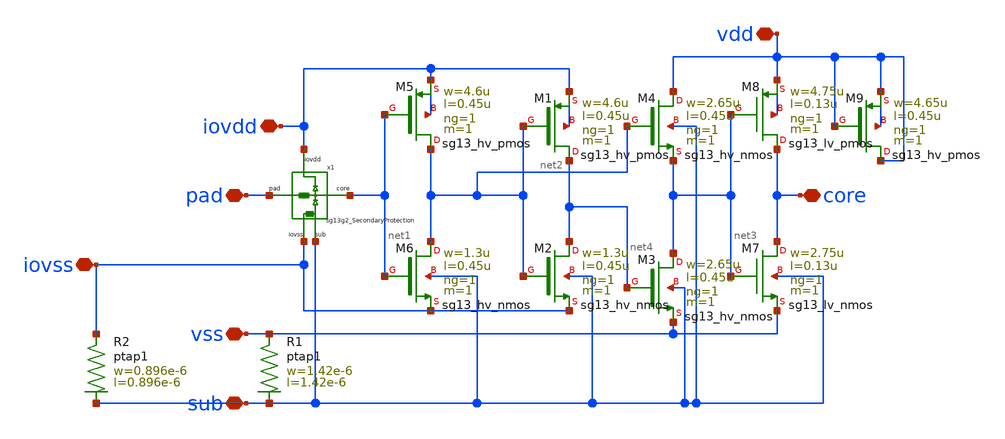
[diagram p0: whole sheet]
** sch_path: MSPHY6034-main/dependencies/unic_cass_2025_team04_padring/xschem/openpdk-libraries/ihp-sg13g2/sg13g2_io/xschem/sg13g2_LevelDown.sch
**.subckt sg13g2_LevelDown iovdd vss core pad vdd iovss sub
*.iopin iovdd
*.iopin vss
*.iopin core
*.iopin pad
*.iopin vdd
*.iopin iovss
*.iopin sub
XR1 vss sub ptap1 R=127.3 w=1.42e-6 l=1.42e-6
XM5 net2 net1 iovdd iovdd sg13_hv_pmos w=4.6u l=0.45u ng=1 m=1 mm_ok=1
XM6 net2 net1 iovss sub sg13_hv_nmos w=1.3u l=0.45u ng=1 m=1 mm_ok=1
XM7 core net3 vss sub sg13_lv_nmos w=2.75u l=0.13u ng=1 m=1 mm_ok=1
XM8 core net3 vdd vdd sg13_lv_pmos w=4.75u l=0.13u ng=1 m=1 mm_ok=1
x1 net1 iovdd iovss pad sub sg13g2_SecondaryProtection
XR2 iovss sub ptap1 R=223.4 w=0.896e-6 l=0.896e-6
XM1 net4 net2 iovdd iovdd sg13_hv_pmos w=4.6u l=0.45u ng=1 m=1 mm_ok=1
XM2 net4 net2 iovss sub sg13_hv_nmos w=1.3u l=0.45u ng=1 m=1 mm_ok=1
XM3 net3 net4 vss sub sg13_hv_nmos w=2.65u l=0.45u ng=1 m=1 mm_ok=1
XM4 vdd net2 net3 sub sg13_hv_nmos w=2.65u l=0.45u ng=1 m=1 mm_ok=1
XM9 vdd vdd vdd vdd sg13_hv_pmos w=4.65u l=0.45u ng=1 m=1 mm_ok=1
**.ends

* expanding   symbol:  sg13g2_SecondaryProtection.sym # of pins=5
** sym_path: MSPHY6034-main/schematic/xschem/openpdk-libraries/ihp-sg13g2/sg13g2_io/xschem/sg13g2_SecondaryProtection.sym
** sch_path: MSPHY6034-main/schematic/xschem/openpdk-libraries/ihp-sg13g2/sg13g2_io/xschem/sg13g2_SecondaryProtection.sch
.subckt sg13g2_SecondaryProtection core iovdd iovss pad sub
*.iopin iovss
*.iopin core
*.iopin pad
*.iopin iovdd
*.iopin sub
XR1 iovss sub ptap1 R=46.56 w=3.005e-6 l=3.005e-6
XD1 core iovdd dpantenna l=4.98u w=0.64u
XD2 sub core dantenna l=3.1u w=0.64u
XR3 pad core sub rppd w=1e-6 l=2e-6 m=1 b=0 mm_ok=1
.ends

.end
